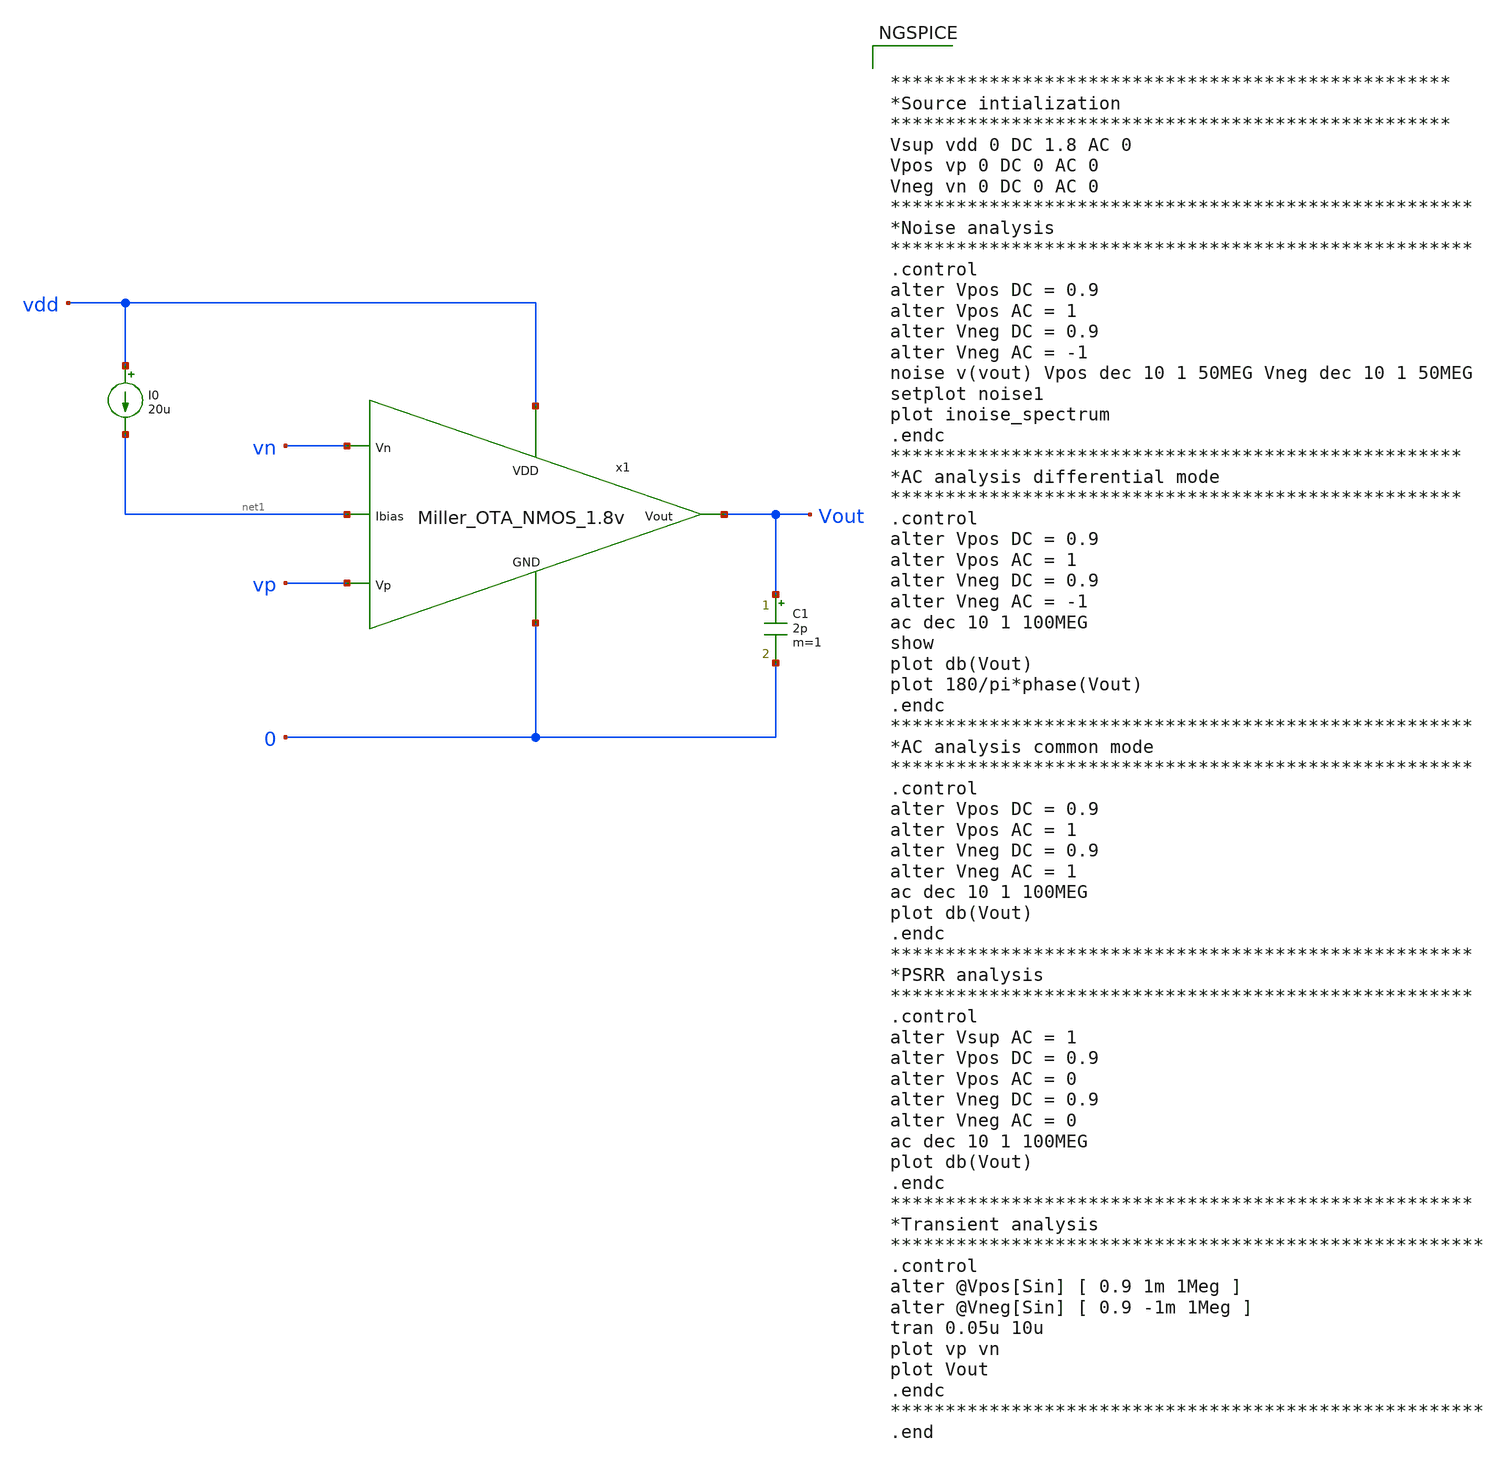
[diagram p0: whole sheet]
** sch_path: Analog_Blocks/OTA/Testbench/Miller_OTA_NMOS_1.8v_TB.sch
**.subckt Miller_OTA_NMOS_1.8v_TB
I0 vdd net1 20u
C1 Vout 0 2p m=1
x1 vdd vn vp Vout net1 0 Miller_OTA_NMOS_1.8v
**** begin user architecture code


***************************************************
*Source intialization
***************************************************
Vsup vdd 0 DC 1.8 AC 0
Vpos vp 0 DC 0 AC 0
Vneg vn 0 DC 0 AC 0
*****************************************************
*Noise analysis
*****************************************************
.control
alter Vpos DC = 0.9
alter Vpos AC = 1
alter Vneg DC = 0.9
alter Vneg AC = -1
noise v(vout) Vpos dec 10 1 50MEG Vneg dec 10 1 50MEG
setplot noise1
plot inoise_spectrum
.endc
****************************************************
*AC analysis differential mode
****************************************************
.control
alter Vpos DC = 0.9
alter Vpos AC = 1
alter Vneg DC = 0.9
alter Vneg AC = -1
ac dec 10 1 100MEG
show
plot db(Vout)
plot 180/pi*phase(Vout)
.endc
*****************************************************
*AC analysis common mode
*****************************************************
.control
alter Vpos DC = 0.9
alter Vpos AC = 1
alter Vneg DC = 0.9
alter Vneg AC = 1
ac dec 10 1 100MEG
plot db(Vout)
.endc
*****************************************************
*PSRR analysis
*****************************************************
.control
alter Vsup AC = 1
alter Vpos DC = 0.9
alter Vpos AC = 0
alter Vneg DC = 0.9
alter Vneg AC = 0
ac dec 10 1 100MEG
plot db(Vout)
.endc
*****************************************************
*Transient analysis
******************************************************
.control
alter @Vpos[Sin] [ 0.9 1m 1Meg ]
alter @Vneg[Sin] [ 0.9 -1m 1Meg ]
tran 0.05u 10u
plot vp vn
plot Vout
.endc
******************************************************
.end



.include $::SKYWATER_MODELS/cells/nfet_01v8/sky130_fd_pr__nfet_01v8__tt.corner.spice
.include $::SKYWATER_MODELS/cells/nfet_01v8_lvt/sky130_fd_pr__nfet_01v8_lvt__tt.corner.spice
.include $::SKYWATER_MODELS/cells/pfet_01v8/sky130_fd_pr__pfet_01v8__tt.corner.spice
.include $::SKYWATER_MODELS/cells/nfet_03v3_nvt/sky130_fd_pr__nfet_03v3_nvt__tt.corner.spice
.include $::SKYWATER_MODELS/cells/nfet_05v0_nvt/sky130_fd_pr__nfet_05v0_nvt__tt.corner.spice
.include $::SKYWATER_MODELS/cells/esd_nfet_01v8/sky130_fd_pr__esd_nfet_01v8__tt.corner.spice
.include $::SKYWATER_MODELS/cells/pfet_01v8_lvt/sky130_fd_pr__pfet_01v8_lvt__tt.corner.spice
.include $::SKYWATER_MODELS/cells/pfet_01v8_hvt/sky130_fd_pr__pfet_01v8_hvt__tt.corner.spice
.include $::SKYWATER_MODELS/cells/esd_pfet_g5v0d10v5/sky130_fd_pr__esd_pfet_g5v0d10v5__tt.corner.spice
.include $::SKYWATER_MODELS/cells/pfet_g5v0d10v5/sky130_fd_pr__pfet_g5v0d10v5__tt.corner.spice
.include $::SKYWATER_MODELS/cells/pfet_g5v0d16v0/sky130_fd_pr__pfet_g5v0d16v0__tt.corner.spice
.include $::SKYWATER_MODELS/cells/nfet_g5v0d10v5/sky130_fd_pr__nfet_g5v0d10v5__tt.corner.spice
.include $::SKYWATER_MODELS/cells/nfet_g5v0d16v0/sky130_fd_pr__nfet_g5v0d16v0__tt_discrete.corner.spice
.include $::SKYWATER_MODELS/cells/esd_nfet_g5v0d10v5/sky130_fd_pr__esd_nfet_g5v0d10v5__tt.corner.spice
.include $::SKYWATER_MODELS/models/corners/tt/nonfet.spice
* Mismatch parameters
.include $::SKYWATER_MODELS/cells/nfet_01v8/sky130_fd_pr__nfet_01v8__mismatch.corner.spice
.include $::SKYWATER_MODELS/cells/pfet_01v8/sky130_fd_pr__pfet_01v8__mismatch.corner.spice
.include $::SKYWATER_MODELS/cells/nfet_01v8_lvt/sky130_fd_pr__nfet_01v8_lvt__mismatch.corner.spice
.include $::SKYWATER_MODELS/cells/pfet_01v8_lvt/sky130_fd_pr__pfet_01v8_lvt__mismatch.corner.spice
.include $::SKYWATER_MODELS/cells/pfet_01v8_hvt/sky130_fd_pr__pfet_01v8_hvt__mismatch.corner.spice
.include $::SKYWATER_MODELS/cells/nfet_g5v0d10v5/sky130_fd_pr__nfet_g5v0d10v5__mismatch.corner.spice
.include $::SKYWATER_MODELS/cells/pfet_g5v0d10v5/sky130_fd_pr__pfet_g5v0d10v5__mismatch.corner.spice
.include $::SKYWATER_MODELS/cells/nfet_05v0_nvt/sky130_fd_pr__nfet_05v0_nvt__mismatch.corner.spice
.include $::SKYWATER_MODELS/cells/nfet_03v3_nvt/sky130_fd_pr__nfet_03v3_nvt__mismatch.corner.spice
* Resistor$::SKYWATER_MODELS/Capacitor
.include $::SKYWATER_MODELS/models/r+c/res_typical__cap_typical.spice
.include $::SKYWATER_MODELS/models/r+c/res_typical__cap_typical__lin.spice
* Special cells
.include $::SKYWATER_MODELS/models/corners/tt/specialized_cells.spice
* All models
.include $::SKYWATER_MODELS/models/all.spice
* Corner
.include $::SKYWATER_MODELS/models/corners/tt/rf.spice

**** end user architecture code
**.ends
.end
